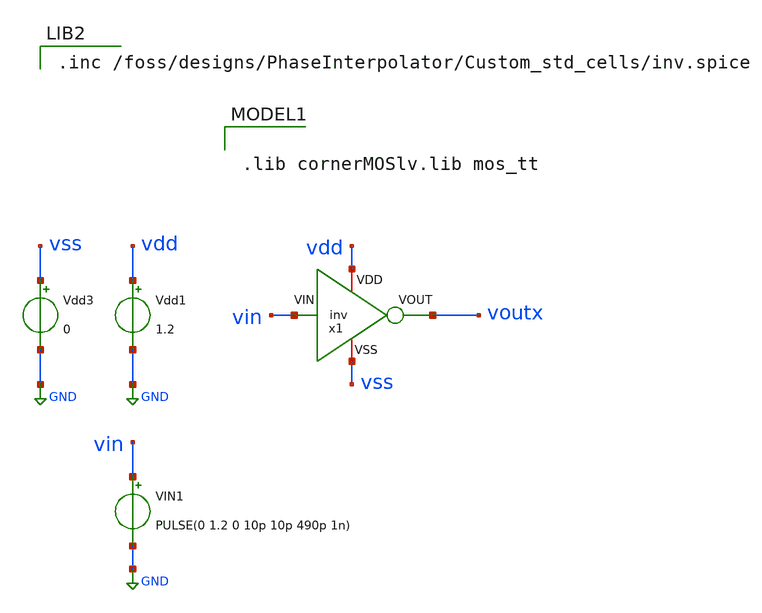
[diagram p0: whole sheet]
** sch_path: verification/testbenches/tb_inv.sch
**.subckt tb_inv
x1 vdd voutx vin vss inv
Vdd1 vdd GND 1.2
Vdd3 vss GND 0
VIN1 vin GND PULSE(0 1.2 0 10p 10p 490p 1n)
**** begin user architecture code


.tran 5p 16n
.save all

.control
run
set color0=white
write inv.raw


.endc



.lib cornerMOSlv.lib mos_tt



.inc /foss/designs/PhaseInterpolator/Custom_std_cells/inv.spice

**** end user architecture code
**.ends
.GLOBAL GND
.end
